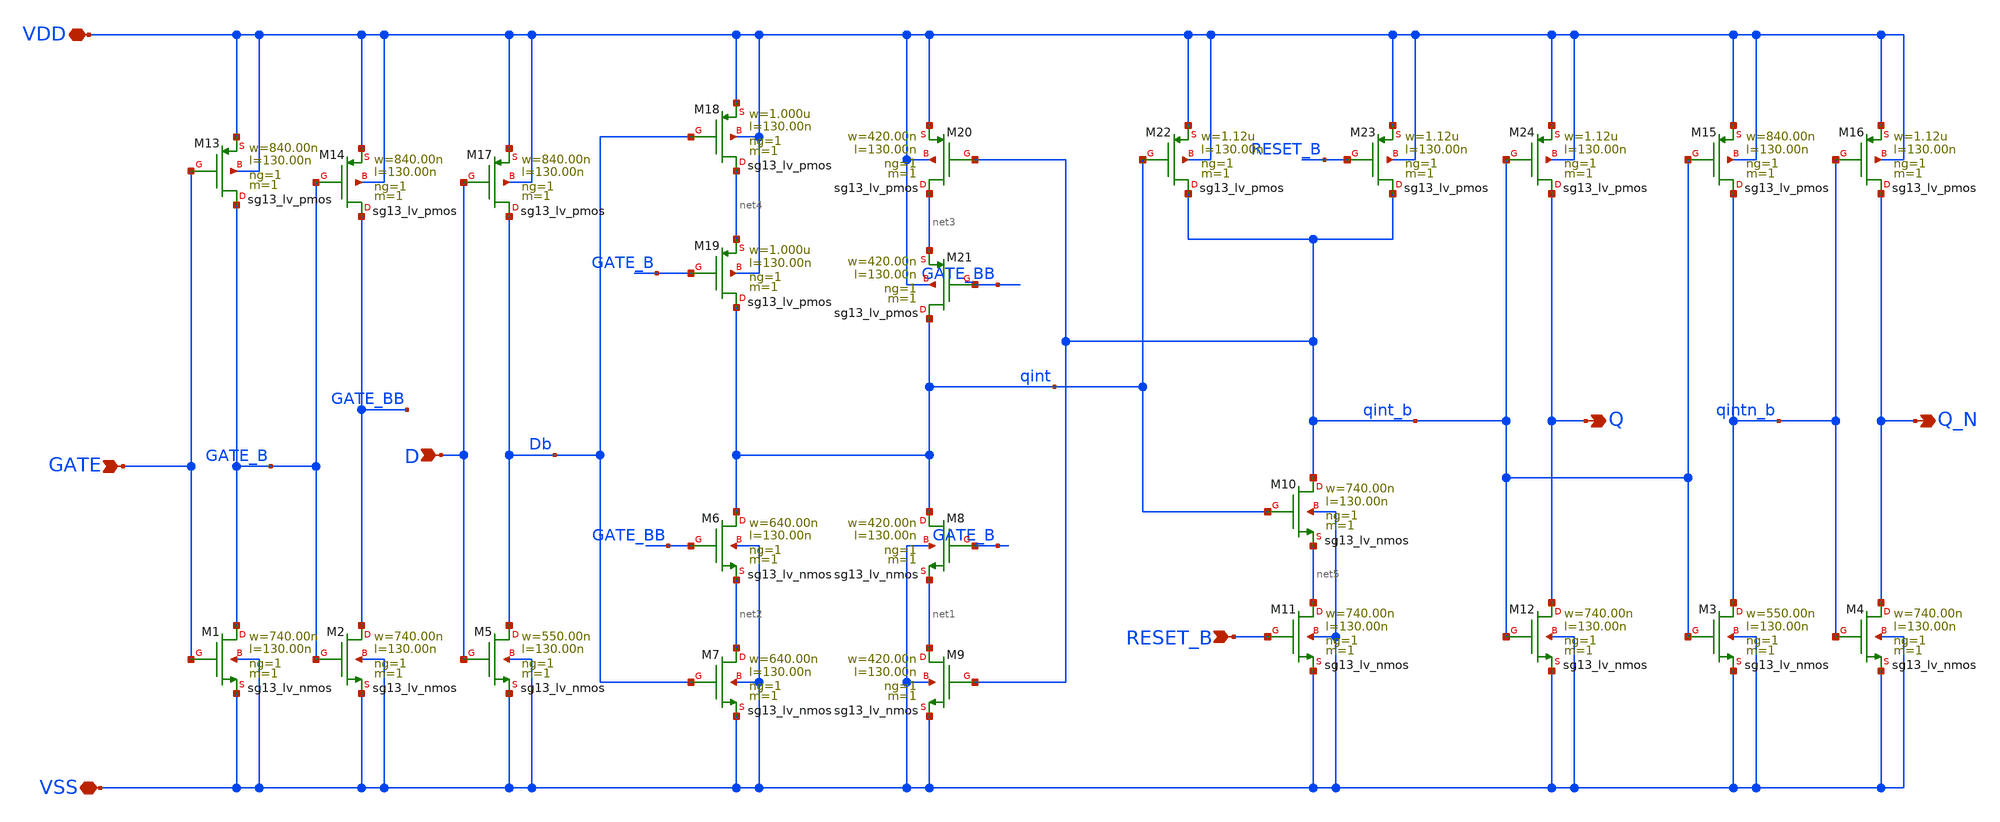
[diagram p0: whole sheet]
** sch_path: ihp-sg13g2/libs.tech/xschem/sg13g2_stdcells/sg13g2_dlhr_1.sch
**.subckt sg13g2_dlhr_1 D GATE RESET_B Q Q_N VDD VSS
*.ipin D
*.ipin GATE
*.ipin RESET_B
*.opin Q
*.opin Q_N
*.iopin VDD
*.iopin VSS
XM1 GATE_B GATE VSS VSS sg13_lv_nmos w=740.00n l=130.00n ng=1 m=1 mm_ok=1
XM2 GATE_BB GATE_B VSS VSS sg13_lv_nmos w=740.00n l=130.00n ng=1 m=1 mm_ok=1
XM3 qintn_b qint_b VSS VSS sg13_lv_nmos w=550.00n l=130.00n ng=1 m=1 mm_ok=1
XM4 Q_N qintn_b VSS VSS sg13_lv_nmos w=740.00n l=130.00n ng=1 m=1 mm_ok=1
XM5 Db D VSS VSS sg13_lv_nmos w=550.00n l=130.00n ng=1 m=1 mm_ok=1
XM6 qint GATE_BB net2 VSS sg13_lv_nmos w=640.00n l=130.00n ng=1 m=1 mm_ok=1
XM7 net2 Db VSS VSS sg13_lv_nmos w=640.00n l=130.00n ng=1 m=1 mm_ok=1
XM8 qint GATE_B net1 VSS sg13_lv_nmos w=420.00n l=130.00n ng=1 m=1 mm_ok=1
XM9 net1 qint_b VSS VSS sg13_lv_nmos w=420.00n l=130.00n ng=1 m=1 mm_ok=1
XM10 qint_b qint net5 VSS sg13_lv_nmos w=740.00n l=130.00n ng=1 m=1 mm_ok=1
XM11 net5 RESET_B VSS VSS sg13_lv_nmos w=740.00n l=130.00n ng=1 m=1 mm_ok=1
XM12 Q qint_b VSS VSS sg13_lv_nmos w=740.00n l=130.00n ng=1 m=1 mm_ok=1
XM13 GATE_B GATE VDD VDD sg13_lv_pmos w=840.00n l=130.00n ng=1 m=1 mm_ok=1
XM14 GATE_BB GATE_B VDD VDD sg13_lv_pmos w=840.00n l=130.00n ng=1 m=1 mm_ok=1
XM15 qintn_b qint_b VDD VDD sg13_lv_pmos w=840.00n l=130.00n ng=1 m=1 mm_ok=1
XM16 Q_N qintn_b VDD VDD sg13_lv_pmos w=1.12u l=130.00n ng=1 m=1 mm_ok=1
XM17 Db D VDD VDD sg13_lv_pmos w=840.00n l=130.00n ng=1 m=1 mm_ok=1
XM18 net4 Db VDD VDD sg13_lv_pmos w=1.000u l=130.00n ng=1 m=1 mm_ok=1
XM19 qint GATE_B net4 VDD sg13_lv_pmos w=1.000u l=130.00n ng=1 m=1 mm_ok=1
XM20 net3 qint_b VDD VDD sg13_lv_pmos w=420.00n l=130.00n ng=1 m=1 mm_ok=1
XM21 qint GATE_BB net3 VDD sg13_lv_pmos w=420.00n l=130.00n ng=1 m=1 mm_ok=1
XM22 qint_b qint VDD VDD sg13_lv_pmos w=1.12u l=130.00n ng=1 m=1 mm_ok=1
XM23 qint_b RESET_B VDD VDD sg13_lv_pmos w=1.12u l=130.00n ng=1 m=1 mm_ok=1
XM24 Q qint_b VDD VDD sg13_lv_pmos w=1.12u l=130.00n ng=1 m=1 mm_ok=1
**.ends
.end
